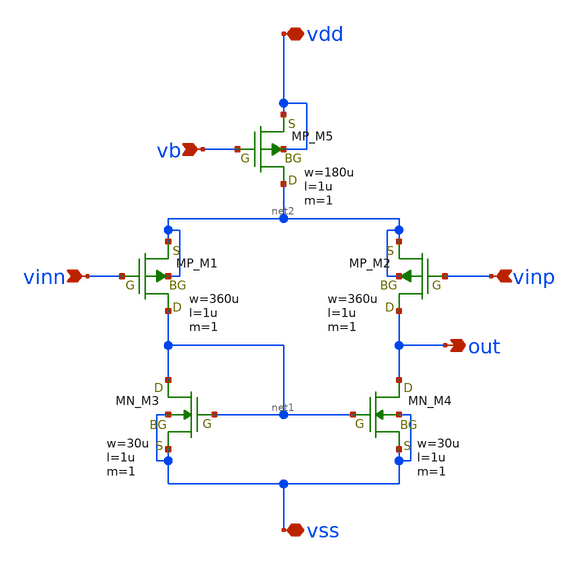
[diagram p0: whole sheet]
** sch_path: OpenSUSI-TR10/opamp/diff_via.sch
**.subckt diff_via vinn vinp vb out vdd vss
*.ipin vinn
*.ipin vinp
*.ipin vb
*.opin out
*.iopin vdd
*.iopin vss
XM5 net2 vb vdd vdd PMOS w=180u l=1u as=0 ad=0 ps=0 pd=0 nrd=0 nrs=0 m=1
XM1 net1 vinn net2 net2 PMOS w=360u l=1u as=0 ad=0 ps=0 pd=0 nrd=0 nrs=0 m=1
XM2 out vinp net2 net2 PMOS w=360u l=1u as=0 ad=0 ps=0 pd=0 nrd=0 nrs=0 m=1
XM3 net1 net1 vss vss NMOS w=30u l=1u as=0 ad=0 ps=0 pd=0 nrd=0 nrs=0 m=1
XM4 out net1 vss vss NMOS w=30u l=1u as=0 ad=0 ps=0 pd=0 nrd=0 nrs=0 m=1
**.ends
.end
